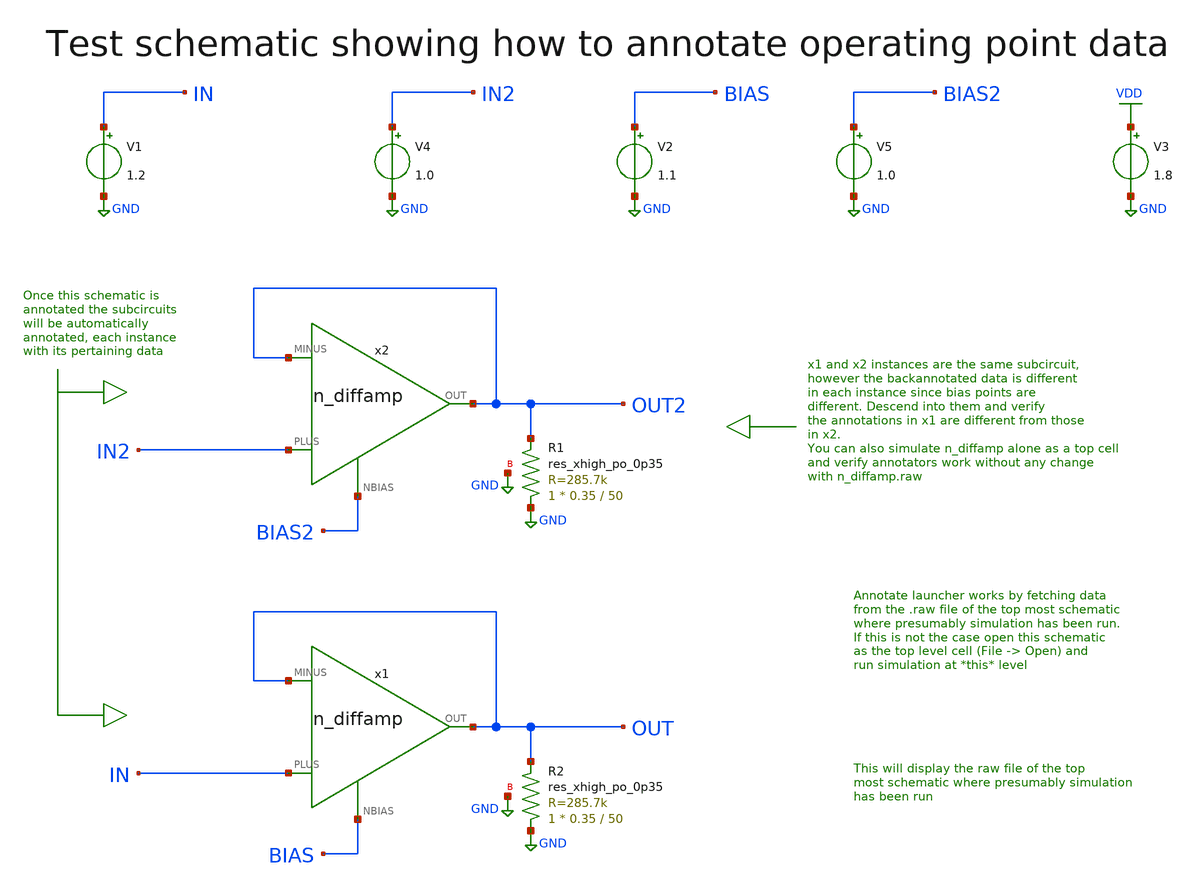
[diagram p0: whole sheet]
** sch_path: sky130A/xschem_libs/sky130_tests/test_analog/schematic/test_analog.sch
* Copyright 2021 Stefan Frederik Schippers
* Licensed under the Apache License, Version 2.0 (the "License");
* you may not use this file except in compliance with the License.
* You may obtain a copy of the License at
* https://www.apache.org/licenses/LICENSE-2.0
* Unless required by applicable law or agreed to in writing, software
* distributed under the License is distributed on an "AS IS" BASIS,
* WITHOUT WARRANTIES OR CONDITIONS OF ANY KIND, either express or implied.
* See the License for the specific language governing permissions and
* limitations under the License.
**.subckt test_analog
x1 OUT OUT IN BIAS n_diffamp
x2 OUT2 OUT2 IN2 BIAS2 n_diffamp
V1 IN GND 1.2
V2 BIAS GND 1.1
V3 VDD GND 1.8
V4 IN2 GND 1.0
V5 BIAS2 GND 1.0
XR1 GND OUT2 GND sky130_fd_pr__res_xhigh_po_0p35 L=50 mult=1 m=1
XR2 GND OUT GND sky130_fd_pr__res_xhigh_po_0p35 L=50 mult=1 m=1
**** begin user architecture code

** opencircuitdesign pdks install
.lib $::SKYWATER_MODELS/sky130.lib.spice tt

**** end user architecture code
**.ends
.GLOBAL GND
.GLOBAL VDD
**** begin user architecture code


* ngspice commands
.options savecurrents
.include test_analog.save
.control
save all
op
print @m.x2.xm5.msky130_fd_pr__nfet_01v8[vth]
write test_analog.raw
* quit 0
.endc



**** end user architecture code
.end
